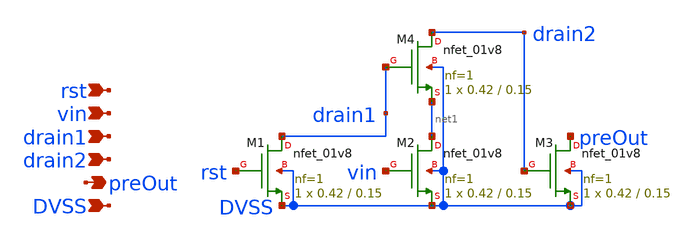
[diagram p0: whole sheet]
** sch_path: xschem/ncell_pfd.sch
**.subckt ncell_pfd rst vin drain1 drain2 preOut DVSS
*.ipin rst
*.ipin vin
*.ipin drain1
*.ipin drain2
*.opin preOut
*.ipin DVSS
XM1 drain1 rst DVSS DVSS sky130_fd_pr__nfet_01v8 L=0.15 W=0.42 nf=1 ad='int((nf+1)/2) * W/nf * 0.29'
+ as='int((nf+2)/2) * W/nf * 0.29' pd='2*int((nf+1)/2) * (W/nf + 0.29)' ps='2*int((nf+2)/2) * (W/nf + 0.29)'
+ nrd='0.29 / W' nrs='0.29 / W' sa=0 sb=0 sd=0 mult=1 m=1
XM2 net1 vin DVSS DVSS sky130_fd_pr__nfet_01v8 L=0.15 W=0.42 nf=1 ad='int((nf+1)/2) * W/nf * 0.29' as='int((nf+2)/2) * W/nf * 0.29'
+ pd='2*int((nf+1)/2) * (W/nf + 0.29)' ps='2*int((nf+2)/2) * (W/nf + 0.29)' nrd='0.29 / W' nrs='0.29 / W'
+ sa=0 sb=0 sd=0 mult=1 m=1
XM3 preOut drain2 DVSS DVSS sky130_fd_pr__nfet_01v8 L=0.15 W=0.42 nf=1 ad='int((nf+1)/2) * W/nf * 0.29'
+ as='int((nf+2)/2) * W/nf * 0.29' pd='2*int((nf+1)/2) * (W/nf + 0.29)' ps='2*int((nf+2)/2) * (W/nf + 0.29)'
+ nrd='0.29 / W' nrs='0.29 / W' sa=0 sb=0 sd=0 mult=1 m=1
XM4 drain2 drain1 net1 DVSS sky130_fd_pr__nfet_01v8 L=0.15 W=0.42 nf=1 ad='int((nf+1)/2) * W/nf * 0.29'
+ as='int((nf+2)/2) * W/nf * 0.29' pd='2*int((nf+1)/2) * (W/nf + 0.29)' ps='2*int((nf+2)/2) * (W/nf + 0.29)'
+ nrd='0.29 / W' nrs='0.29 / W' sa=0 sb=0 sd=0 mult=1 m=1
**.ends
.end
